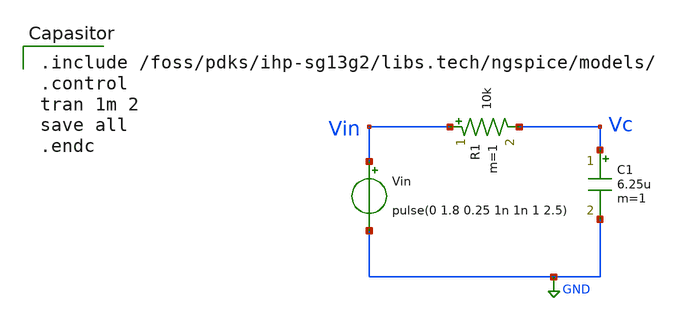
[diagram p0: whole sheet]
** sch_path: content/simulation_files/xschem/02_Capasitor.sch
**.subckt 02_Capasitor
Vin Vin GND pulse(0 1.8 0.25 1n 1n 1 2.5)
R1 Vin Vc 10k m=1
C1 Vc GND 6.25u m=1
**** begin user architecture code

.include /foss/pdks/ihp-sg13g2/libs.tech/ngspice/models/
.control
tran 1m 2
save all
.endc

**** end user architecture code
**.ends
.GLOBAL GND
.end
